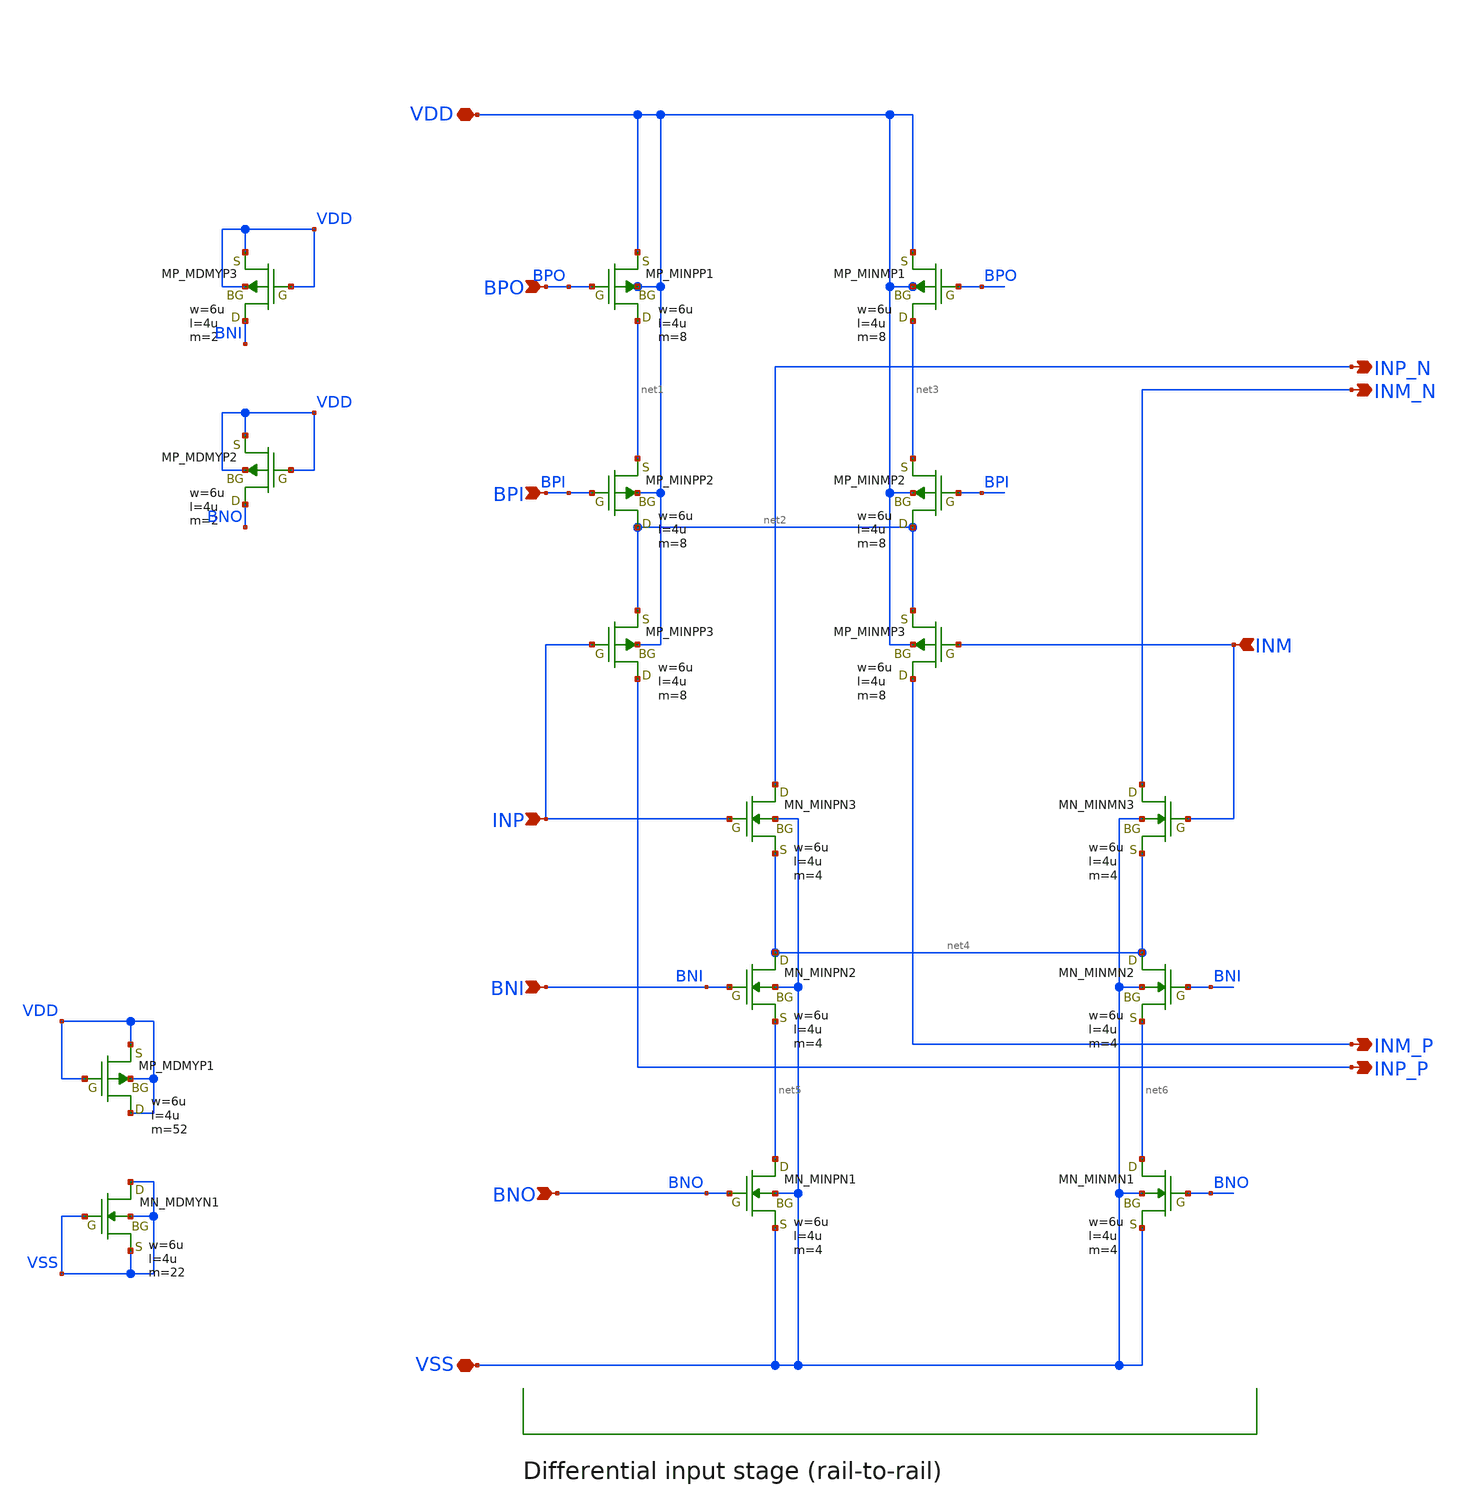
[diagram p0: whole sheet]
** sch_path: OpenSUSI-TR10/opamp_r2r_audio/opamp_r2r_diff_dummypoly.sch
**.subckt opamp_r2r_diff_dummypoly VDD VSS INP INM INP_N INM_N INM_P INP_P BPO BPI BNI BNO
*.iopin VDD
*.iopin VSS
*.ipin INP
*.ipin INM
*.opin INP_N
*.opin INM_N
*.opin INM_P
*.opin INP_P
*.ipin BPO
*.ipin BPI
*.ipin BNI
*.ipin BNO
XMINPP1 net1 BPO VDD VDD PMOS w=6u l=4u as=0 ad=0 ps=0 pd=0 nrd=0 nrs=0 m=8
XMINPP2 net2 BPI net1 VDD PMOS w=6u l=4u as=0 ad=0 ps=0 pd=0 nrd=0 nrs=0 m=8
XMINPP3 INP_P INP net2 VDD PMOS w=6u l=4u as=0 ad=0 ps=0 pd=0 nrd=0 nrs=0 m=8
XMINMP1 net3 BPO VDD VDD PMOS w=6u l=4u as=0 ad=0 ps=0 pd=0 nrd=0 nrs=0 m=8
XMINMP2 net2 BPI net3 VDD PMOS w=6u l=4u as=0 ad=0 ps=0 pd=0 nrd=0 nrs=0 m=8
XMINMP3 INM_P INM net2 VDD PMOS w=6u l=4u as=0 ad=0 ps=0 pd=0 nrd=0 nrs=0 m=8
XMINPN2 net4 BNI net5 VSS NMOS w=6u l=4u as=0 ad=0 ps=0 pd=0 nrd=0 nrs=0 m=4
XMINPN1 net5 BNO VSS VSS NMOS w=6u l=4u as=0 ad=0 ps=0 pd=0 nrd=0 nrs=0 m=4
XMINPN3 INP_N INP net4 VSS NMOS w=6u l=4u as=0 ad=0 ps=0 pd=0 nrd=0 nrs=0 m=4
XMINMN2 net4 BNI net6 VSS NMOS w=6u l=4u as=0 ad=0 ps=0 pd=0 nrd=0 nrs=0 m=4
XMINMN1 net6 BNO VSS VSS NMOS w=6u l=4u as=0 ad=0 ps=0 pd=0 nrd=0 nrs=0 m=4
XMINMN3 INM_N INM net4 VSS NMOS w=6u l=4u as=0 ad=0 ps=0 pd=0 nrd=0 nrs=0 m=4
XMDMYN1 VSS VSS VSS VSS NMOS w=6u l=4u as=0 ad=0 ps=0 pd=0 nrd=0 nrs=0 m=22
XMDMYP1 VDD VDD VDD VDD PMOS w=6u l=4u as=0 ad=0 ps=0 pd=0 nrd=0 nrs=0 m=52
XMDMYP2 BNO VDD VDD VDD PMOS w=6u l=4u as=0 ad=0 ps=0 pd=0 nrd=0 nrs=0 m=2
XMDMYP3 BNI VDD VDD VDD PMOS w=6u l=4u as=0 ad=0 ps=0 pd=0 nrd=0 nrs=0 m=2
**.ends
.end
